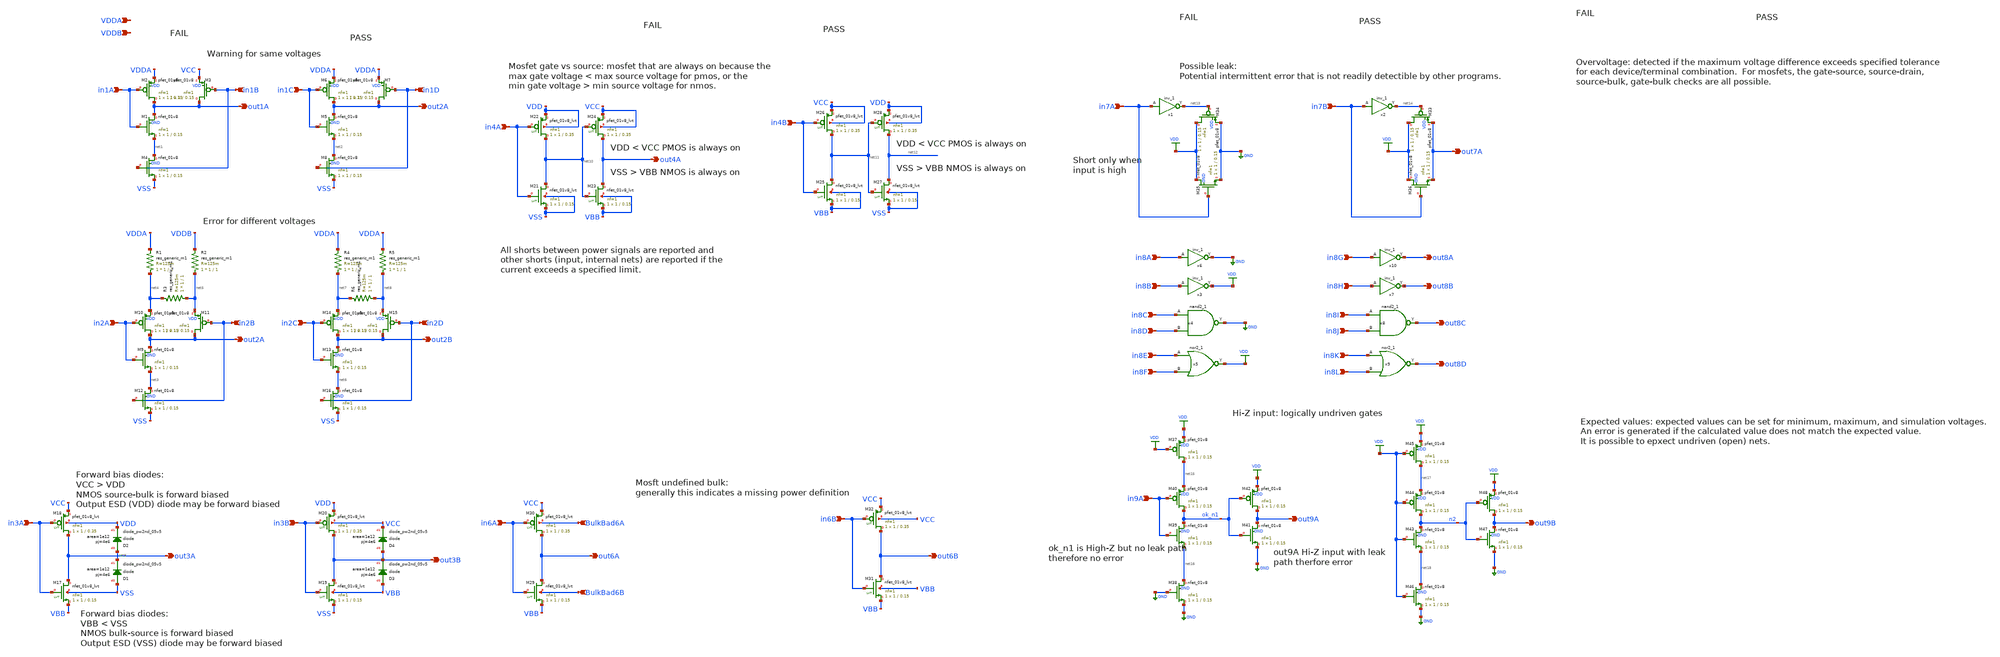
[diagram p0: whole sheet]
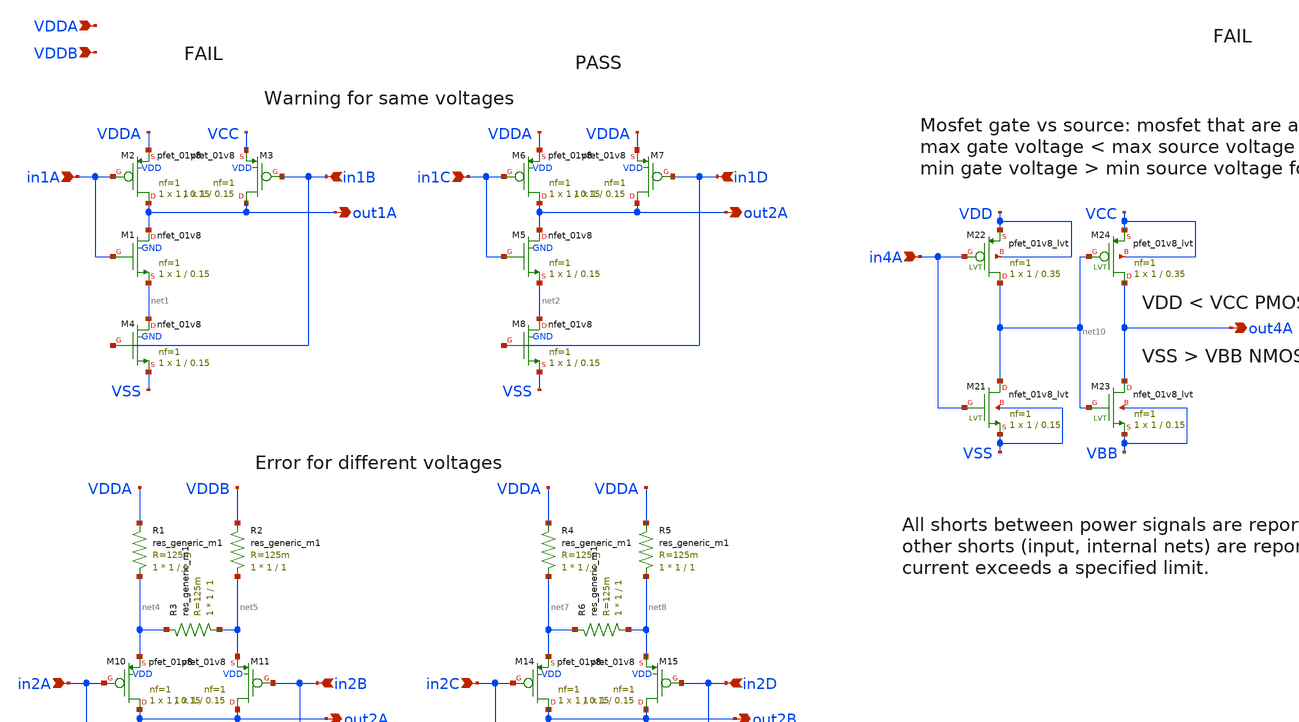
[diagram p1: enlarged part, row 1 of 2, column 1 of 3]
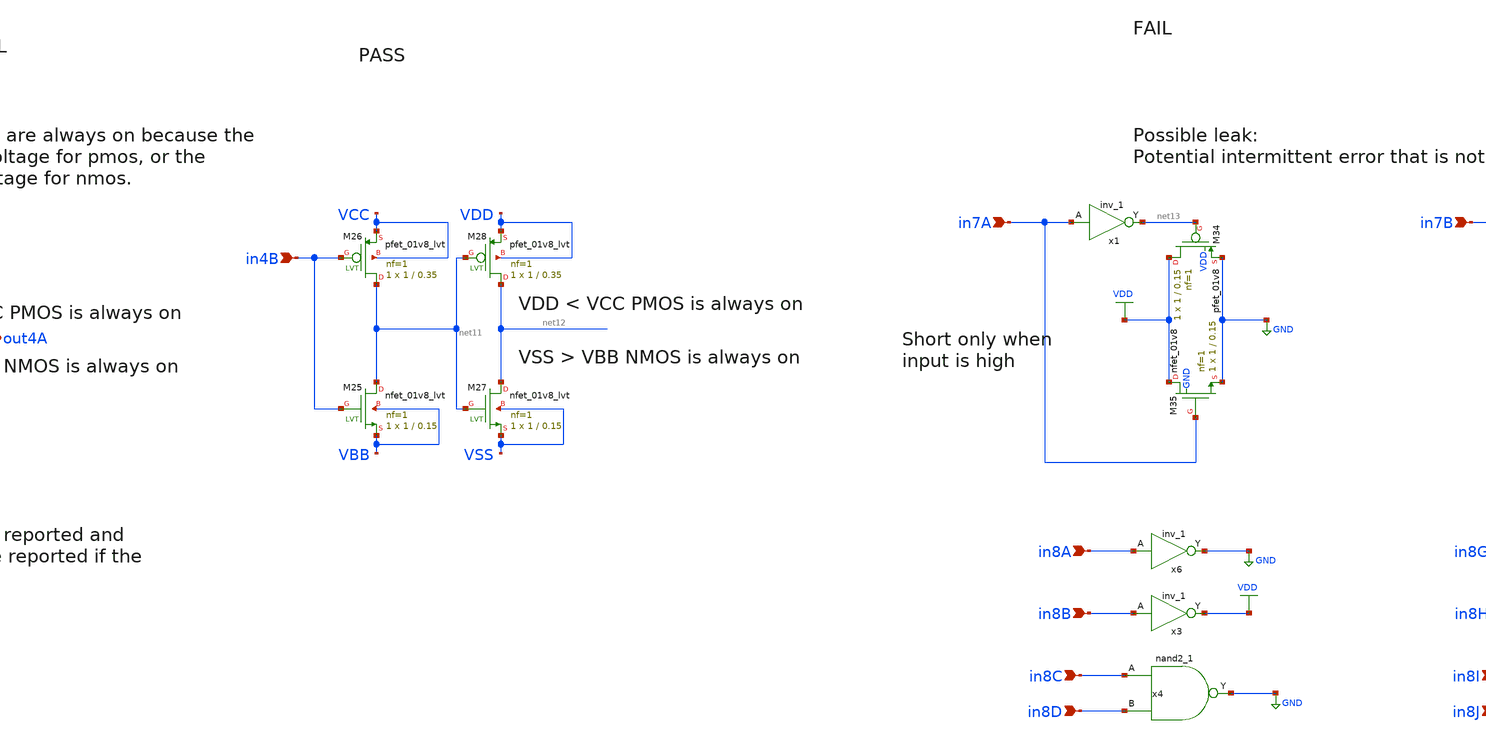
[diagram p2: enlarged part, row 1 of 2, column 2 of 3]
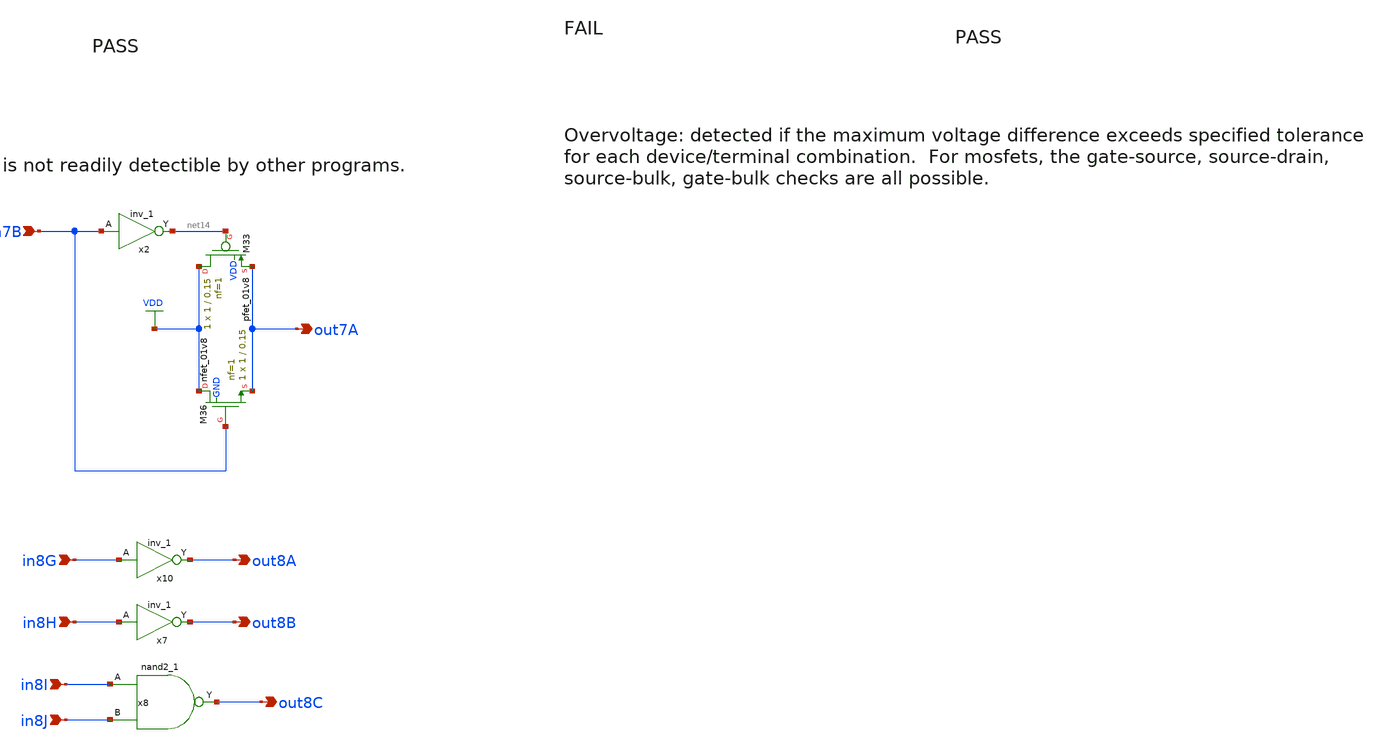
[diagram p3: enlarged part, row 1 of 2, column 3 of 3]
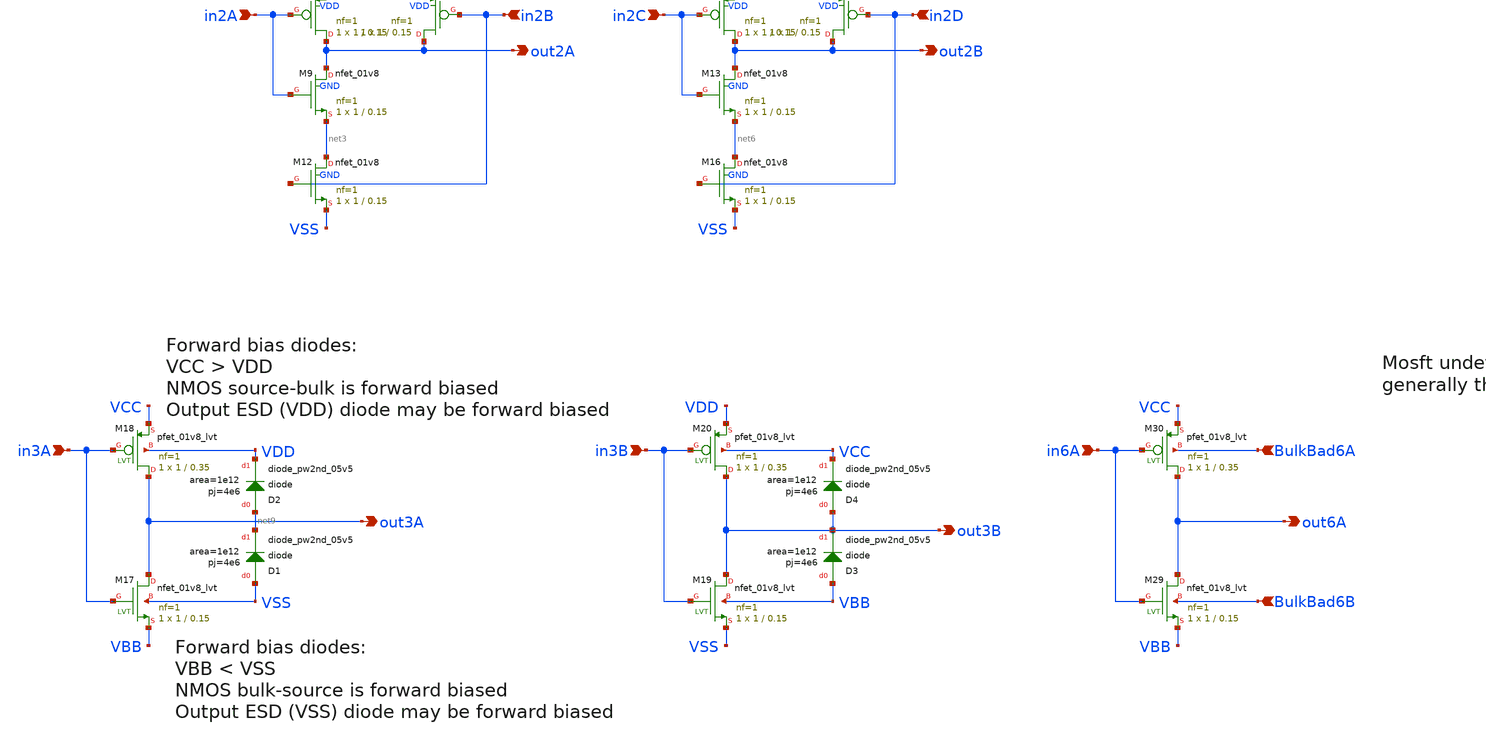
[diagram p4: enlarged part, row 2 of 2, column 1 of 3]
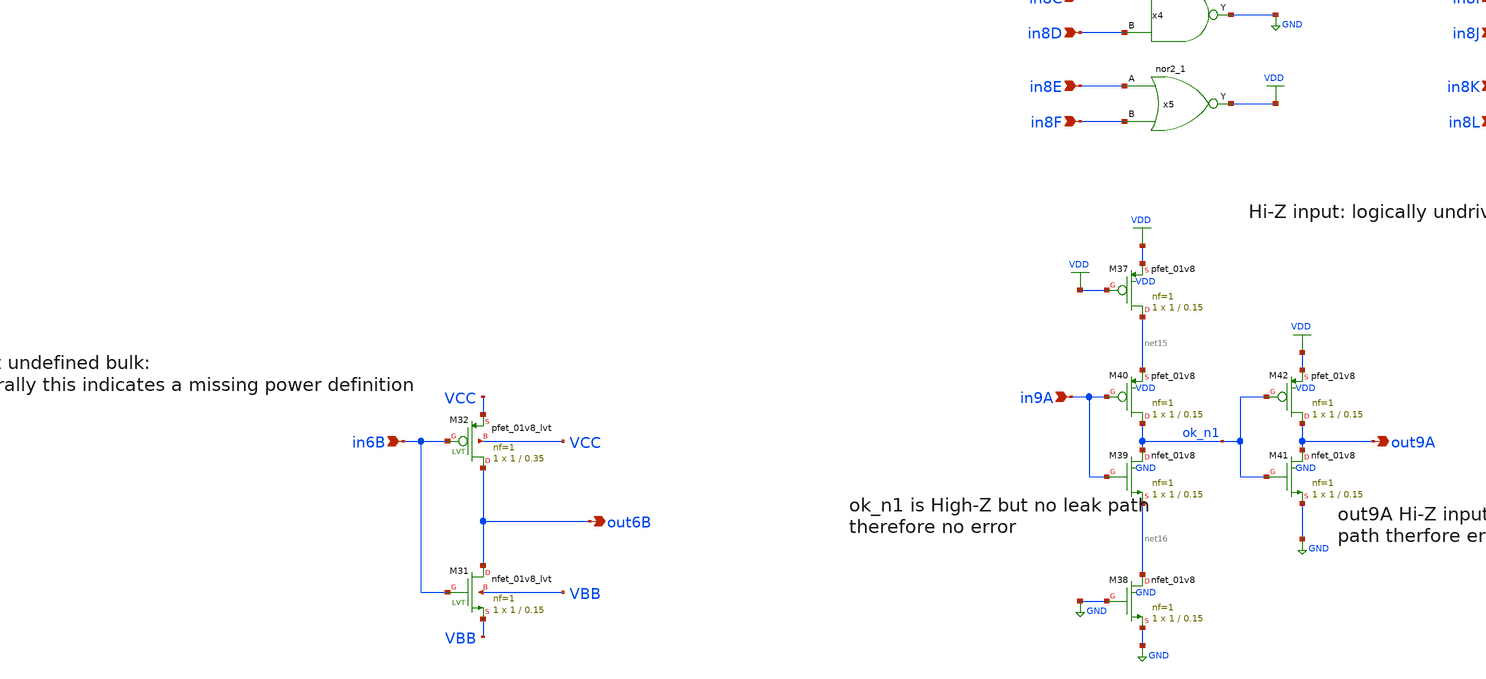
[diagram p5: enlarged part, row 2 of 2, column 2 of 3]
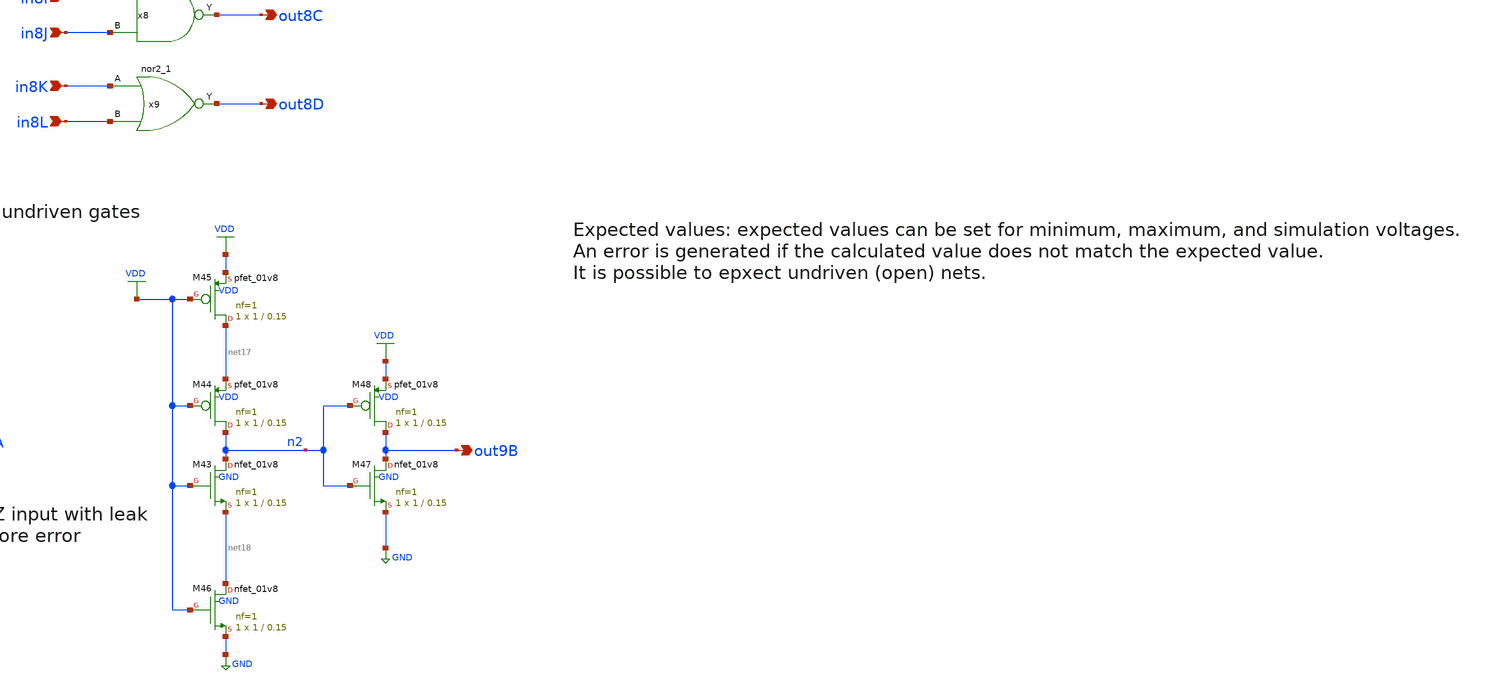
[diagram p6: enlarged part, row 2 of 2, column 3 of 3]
** sch_path: src/xe/test_cases/cvc_errors.sch
**.subckt cvc_errors in1A in1B in1C in1D in2A in2B in2C in2D out1A out2A out3A out2B in3A in3B out2A
*+ out3B in4A out4A in4B out7A in6A in6B out6A out6B in7A in7B in8A in8B in8C in8D in8E in8F in8G in8H in8I
*+ in8J in8K in8L out8A out8B out8C out8D in9A out9A out9B BulkBad6A BulkBad6B VDDB VDDA
*.ipin in1A
*.ipin in1B
*.ipin in1C
*.ipin in1D
*.ipin in2A
*.ipin in2B
*.ipin in2C
*.ipin in2D
*.opin out1A
*.opin out2A
*.opin out3A
*.opin out2B
*.ipin in3A
*.ipin in3B
*.opin out2A
*.opin out3B
*.ipin in4A
*.opin out4A
*.ipin in4B
*.opin out7A
*.ipin in6A
*.ipin in6B
*.opin out6A
*.opin out6B
*.ipin in7A
*.ipin in7B
*.ipin in8A
*.ipin in8B
*.ipin in8C
*.ipin in8D
*.ipin in8E
*.ipin in8F
*.ipin in8G
*.ipin in8H
*.ipin in8I
*.ipin in8J
*.ipin in8K
*.ipin in8L
*.opin out8A
*.opin out8B
*.opin out8C
*.opin out8D
*.ipin in9A
*.opin out9A
*.opin out9B
*.ipin BulkBad6A
*.ipin BulkBad6B
*.ipin VDDB
*.ipin VDDA
XM1 out1A in1A net1 GND sky130_fd_pr__nfet_01v8 L=0.15 W=1 nf=1 ad='int((nf+1)/2) * W/nf * 0.29' as='int((nf+2)/2) * W/nf * 0.29'
+ pd='2*int((nf+1)/2) * (W/nf + 0.29)' ps='2*int((nf+2)/2) * (W/nf + 0.29)' nrd='0.29 / W' nrs='0.29 / W'
+ sa=0 sb=0 sd=0 mult=1 m=1
XM2 out1A in1A VDDA VDD sky130_fd_pr__pfet_01v8 L=0.15 W=1 nf=1 ad='int((nf+1)/2) * W/nf * 0.29' as='int((nf+2)/2) * W/nf * 0.29'
+ pd='2*int((nf+1)/2) * (W/nf + 0.29)' ps='2*int((nf+2)/2) * (W/nf + 0.29)' nrd='0.29 / W' nrs='0.29 / W'
+ sa=0 sb=0 sd=0 mult=1 m=1
XM3 out1A in1B VCC VDD sky130_fd_pr__pfet_01v8 L=0.15 W=1 nf=1 ad='int((nf+1)/2) * W/nf * 0.29' as='int((nf+2)/2) * W/nf * 0.29'
+ pd='2*int((nf+1)/2) * (W/nf + 0.29)' ps='2*int((nf+2)/2) * (W/nf + 0.29)' nrd='0.29 / W' nrs='0.29 / W'
+ sa=0 sb=0 sd=0 mult=1 m=1
XM4 net1 in1B VSS GND sky130_fd_pr__nfet_01v8 L=0.15 W=1 nf=1 ad='int((nf+1)/2) * W/nf * 0.29' as='int((nf+2)/2) * W/nf * 0.29'
+ pd='2*int((nf+1)/2) * (W/nf + 0.29)' ps='2*int((nf+2)/2) * (W/nf + 0.29)' nrd='0.29 / W' nrs='0.29 / W'
+ sa=0 sb=0 sd=0 mult=1 m=1
XM5 out2A in1C net2 GND sky130_fd_pr__nfet_01v8 L=0.15 W=1 nf=1 ad='int((nf+1)/2) * W/nf * 0.29' as='int((nf+2)/2) * W/nf * 0.29'
+ pd='2*int((nf+1)/2) * (W/nf + 0.29)' ps='2*int((nf+2)/2) * (W/nf + 0.29)' nrd='0.29 / W' nrs='0.29 / W'
+ sa=0 sb=0 sd=0 mult=1 m=1
XM6 out2A in1C VDDA VDD sky130_fd_pr__pfet_01v8 L=0.15 W=1 nf=1 ad='int((nf+1)/2) * W/nf * 0.29' as='int((nf+2)/2) * W/nf * 0.29'
+ pd='2*int((nf+1)/2) * (W/nf + 0.29)' ps='2*int((nf+2)/2) * (W/nf + 0.29)' nrd='0.29 / W' nrs='0.29 / W'
+ sa=0 sb=0 sd=0 mult=1 m=1
XM7 out2A in1D VDDA VDD sky130_fd_pr__pfet_01v8 L=0.15 W=1 nf=1 ad='int((nf+1)/2) * W/nf * 0.29' as='int((nf+2)/2) * W/nf * 0.29'
+ pd='2*int((nf+1)/2) * (W/nf + 0.29)' ps='2*int((nf+2)/2) * (W/nf + 0.29)' nrd='0.29 / W' nrs='0.29 / W'
+ sa=0 sb=0 sd=0 mult=1 m=1
XM8 net2 in1D VSS GND sky130_fd_pr__nfet_01v8 L=0.15 W=1 nf=1 ad='int((nf+1)/2) * W/nf * 0.29' as='int((nf+2)/2) * W/nf * 0.29'
+ pd='2*int((nf+1)/2) * (W/nf + 0.29)' ps='2*int((nf+2)/2) * (W/nf + 0.29)' nrd='0.29 / W' nrs='0.29 / W'
+ sa=0 sb=0 sd=0 mult=1 m=1
R1 net4 VDDA sky130_fd_pr__res_generic_m1 W=1 L=1 m=1
XM9 out2A in2A net3 GND sky130_fd_pr__nfet_01v8 L=0.15 W=1 nf=1 ad='int((nf+1)/2) * W/nf * 0.29' as='int((nf+2)/2) * W/nf * 0.29'
+ pd='2*int((nf+1)/2) * (W/nf + 0.29)' ps='2*int((nf+2)/2) * (W/nf + 0.29)' nrd='0.29 / W' nrs='0.29 / W'
+ sa=0 sb=0 sd=0 mult=1 m=1
XM10 out2A in2A net4 VDD sky130_fd_pr__pfet_01v8 L=0.15 W=1 nf=1 ad='int((nf+1)/2) * W/nf * 0.29' as='int((nf+2)/2) * W/nf * 0.29'
+ pd='2*int((nf+1)/2) * (W/nf + 0.29)' ps='2*int((nf+2)/2) * (W/nf + 0.29)' nrd='0.29 / W' nrs='0.29 / W'
+ sa=0 sb=0 sd=0 mult=1 m=1
XM11 out2A in2B net5 VDD sky130_fd_pr__pfet_01v8 L=0.15 W=1 nf=1 ad='int((nf+1)/2) * W/nf * 0.29' as='int((nf+2)/2) * W/nf * 0.29'
+ pd='2*int((nf+1)/2) * (W/nf + 0.29)' ps='2*int((nf+2)/2) * (W/nf + 0.29)' nrd='0.29 / W' nrs='0.29 / W'
+ sa=0 sb=0 sd=0 mult=1 m=1
XM12 net3 in2B VSS GND sky130_fd_pr__nfet_01v8 L=0.15 W=1 nf=1 ad='int((nf+1)/2) * W/nf * 0.29' as='int((nf+2)/2) * W/nf * 0.29'
+ pd='2*int((nf+1)/2) * (W/nf + 0.29)' ps='2*int((nf+2)/2) * (W/nf + 0.29)' nrd='0.29 / W' nrs='0.29 / W'
+ sa=0 sb=0 sd=0 mult=1 m=1
R2 net5 VDDB sky130_fd_pr__res_generic_m1 W=1 L=1 m=1
R3 net5 net4 sky130_fd_pr__res_generic_m1 W=1 L=1 m=1
R4 net7 VDDA sky130_fd_pr__res_generic_m1 W=1 L=1 m=1
XM13 out2B in2C net6 GND sky130_fd_pr__nfet_01v8 L=0.15 W=1 nf=1 ad='int((nf+1)/2) * W/nf * 0.29' as='int((nf+2)/2) * W/nf * 0.29'
+ pd='2*int((nf+1)/2) * (W/nf + 0.29)' ps='2*int((nf+2)/2) * (W/nf + 0.29)' nrd='0.29 / W' nrs='0.29 / W'
+ sa=0 sb=0 sd=0 mult=1 m=1
XM14 out2B in2C net7 VDD sky130_fd_pr__pfet_01v8 L=0.15 W=1 nf=1 ad='int((nf+1)/2) * W/nf * 0.29' as='int((nf+2)/2) * W/nf * 0.29'
+ pd='2*int((nf+1)/2) * (W/nf + 0.29)' ps='2*int((nf+2)/2) * (W/nf + 0.29)' nrd='0.29 / W' nrs='0.29 / W'
+ sa=0 sb=0 sd=0 mult=1 m=1
XM15 out2B in2D net8 VDD sky130_fd_pr__pfet_01v8 L=0.15 W=1 nf=1 ad='int((nf+1)/2) * W/nf * 0.29' as='int((nf+2)/2) * W/nf * 0.29'
+ pd='2*int((nf+1)/2) * (W/nf + 0.29)' ps='2*int((nf+2)/2) * (W/nf + 0.29)' nrd='0.29 / W' nrs='0.29 / W'
+ sa=0 sb=0 sd=0 mult=1 m=1
XM16 net6 in2D VSS GND sky130_fd_pr__nfet_01v8 L=0.15 W=1 nf=1 ad='int((nf+1)/2) * W/nf * 0.29' as='int((nf+2)/2) * W/nf * 0.29'
+ pd='2*int((nf+1)/2) * (W/nf + 0.29)' ps='2*int((nf+2)/2) * (W/nf + 0.29)' nrd='0.29 / W' nrs='0.29 / W'
+ sa=0 sb=0 sd=0 mult=1 m=1
R5 net8 VDDA sky130_fd_pr__res_generic_m1 W=1 L=1 m=1
R6 net8 net7 sky130_fd_pr__res_generic_m1 W=1 L=1 m=1
XM17 out3A in3A VBB VSS sky130_fd_pr__nfet_01v8_lvt L=0.15 W=1 nf=1 ad='int((nf+1)/2) * W/nf * 0.29'
+ as='int((nf+2)/2) * W/nf * 0.29' pd='2*int((nf+1)/2) * (W/nf + 0.29)' ps='2*int((nf+2)/2) * (W/nf + 0.29)'
+ nrd='0.29 / W' nrs='0.29 / W' sa=0 sb=0 sd=0 mult=1 m=1
XM18 out3A in3A VCC VDD sky130_fd_pr__pfet_01v8_lvt L=0.35 W=1 nf=1 ad='int((nf+1)/2) * W/nf * 0.29'
+ as='int((nf+2)/2) * W/nf * 0.29' pd='2*int((nf+1)/2) * (W/nf + 0.29)' ps='2*int((nf+2)/2) * (W/nf + 0.29)'
+ nrd='0.29 / W' nrs='0.29 / W' sa=0 sb=0 sd=0 mult=1 m=1
XD1 VSS net9 sky130_fd_pr__diode_pw2nd_05v5 area=1e12 pj=4e6
XD2 net9 VDD sky130_fd_pr__diode_pw2nd_05v5 area=1e12 pj=4e6
XM19 out3B in3B VSS VBB sky130_fd_pr__nfet_01v8_lvt L=0.15 W=1 nf=1 ad='int((nf+1)/2) * W/nf * 0.29'
+ as='int((nf+2)/2) * W/nf * 0.29' pd='2*int((nf+1)/2) * (W/nf + 0.29)' ps='2*int((nf+2)/2) * (W/nf + 0.29)'
+ nrd='0.29 / W' nrs='0.29 / W' sa=0 sb=0 sd=0 mult=1 m=1
XM20 out3B in3B VDD VCC sky130_fd_pr__pfet_01v8_lvt L=0.35 W=1 nf=1 ad='int((nf+1)/2) * W/nf * 0.29'
+ as='int((nf+2)/2) * W/nf * 0.29' pd='2*int((nf+1)/2) * (W/nf + 0.29)' ps='2*int((nf+2)/2) * (W/nf + 0.29)'
+ nrd='0.29 / W' nrs='0.29 / W' sa=0 sb=0 sd=0 mult=1 m=1
XD3 VBB out3B sky130_fd_pr__diode_pw2nd_05v5 area=1e12 pj=4e6
XD4 out3B VCC sky130_fd_pr__diode_pw2nd_05v5 area=1e12 pj=4e6
XM21 net10 in4A VSS VSS sky130_fd_pr__nfet_01v8_lvt L=0.15 W=1 nf=1 ad='int((nf+1)/2) * W/nf * 0.29'
+ as='int((nf+2)/2) * W/nf * 0.29' pd='2*int((nf+1)/2) * (W/nf + 0.29)' ps='2*int((nf+2)/2) * (W/nf + 0.29)'
+ nrd='0.29 / W' nrs='0.29 / W' sa=0 sb=0 sd=0 mult=1 m=1
XM22 net10 in4A VDD VDD sky130_fd_pr__pfet_01v8_lvt L=0.35 W=1 nf=1 ad='int((nf+1)/2) * W/nf * 0.29'
+ as='int((nf+2)/2) * W/nf * 0.29' pd='2*int((nf+1)/2) * (W/nf + 0.29)' ps='2*int((nf+2)/2) * (W/nf + 0.29)'
+ nrd='0.29 / W' nrs='0.29 / W' sa=0 sb=0 sd=0 mult=1 m=1
XM23 out4A net10 VBB VBB sky130_fd_pr__nfet_01v8_lvt L=0.15 W=1 nf=1 ad='int((nf+1)/2) * W/nf * 0.29'
+ as='int((nf+2)/2) * W/nf * 0.29' pd='2*int((nf+1)/2) * (W/nf + 0.29)' ps='2*int((nf+2)/2) * (W/nf + 0.29)'
+ nrd='0.29 / W' nrs='0.29 / W' sa=0 sb=0 sd=0 mult=1 m=1
XM24 out4A net10 VCC VCC sky130_fd_pr__pfet_01v8_lvt L=0.35 W=1 nf=1 ad='int((nf+1)/2) * W/nf * 0.29'
+ as='int((nf+2)/2) * W/nf * 0.29' pd='2*int((nf+1)/2) * (W/nf + 0.29)' ps='2*int((nf+2)/2) * (W/nf + 0.29)'
+ nrd='0.29 / W' nrs='0.29 / W' sa=0 sb=0 sd=0 mult=1 m=1
XM25 net11 in4B VBB VBB sky130_fd_pr__nfet_01v8_lvt L=0.15 W=1 nf=1 ad='int((nf+1)/2) * W/nf * 0.29'
+ as='int((nf+2)/2) * W/nf * 0.29' pd='2*int((nf+1)/2) * (W/nf + 0.29)' ps='2*int((nf+2)/2) * (W/nf + 0.29)'
+ nrd='0.29 / W' nrs='0.29 / W' sa=0 sb=0 sd=0 mult=1 m=1
XM26 net11 in4B VCC VCC sky130_fd_pr__pfet_01v8_lvt L=0.35 W=1 nf=1 ad='int((nf+1)/2) * W/nf * 0.29'
+ as='int((nf+2)/2) * W/nf * 0.29' pd='2*int((nf+1)/2) * (W/nf + 0.29)' ps='2*int((nf+2)/2) * (W/nf + 0.29)'
+ nrd='0.29 / W' nrs='0.29 / W' sa=0 sb=0 sd=0 mult=1 m=1
XM27 net12 net11 VSS VSS sky130_fd_pr__nfet_01v8_lvt L=0.15 W=1 nf=1 ad='int((nf+1)/2) * W/nf * 0.29'
+ as='int((nf+2)/2) * W/nf * 0.29' pd='2*int((nf+1)/2) * (W/nf + 0.29)' ps='2*int((nf+2)/2) * (W/nf + 0.29)'
+ nrd='0.29 / W' nrs='0.29 / W' sa=0 sb=0 sd=0 mult=1 m=1
XM28 net12 net11 VDD VDD sky130_fd_pr__pfet_01v8_lvt L=0.35 W=1 nf=1 ad='int((nf+1)/2) * W/nf * 0.29'
+ as='int((nf+2)/2) * W/nf * 0.29' pd='2*int((nf+1)/2) * (W/nf + 0.29)' ps='2*int((nf+2)/2) * (W/nf + 0.29)'
+ nrd='0.29 / W' nrs='0.29 / W' sa=0 sb=0 sd=0 mult=1 m=1
XM29 out6A in6A VBB BulkBad6B sky130_fd_pr__nfet_01v8_lvt L=0.15 W=1 nf=1 ad='int((nf+1)/2) * W/nf * 0.29'
+ as='int((nf+2)/2) * W/nf * 0.29' pd='2*int((nf+1)/2) * (W/nf + 0.29)' ps='2*int((nf+2)/2) * (W/nf + 0.29)'
+ nrd='0.29 / W' nrs='0.29 / W' sa=0 sb=0 sd=0 mult=1 m=1
XM30 out6A in6A VCC BulkBad6A sky130_fd_pr__pfet_01v8_lvt L=0.35 W=1 nf=1 ad='int((nf+1)/2) * W/nf * 0.29'
+ as='int((nf+2)/2) * W/nf * 0.29' pd='2*int((nf+1)/2) * (W/nf + 0.29)' ps='2*int((nf+2)/2) * (W/nf + 0.29)'
+ nrd='0.29 / W' nrs='0.29 / W' sa=0 sb=0 sd=0 mult=1 m=1
XM31 out6B in6B VBB VBB sky130_fd_pr__nfet_01v8_lvt L=0.15 W=1 nf=1 ad='int((nf+1)/2) * W/nf * 0.29'
+ as='int((nf+2)/2) * W/nf * 0.29' pd='2*int((nf+1)/2) * (W/nf + 0.29)' ps='2*int((nf+2)/2) * (W/nf + 0.29)'
+ nrd='0.29 / W' nrs='0.29 / W' sa=0 sb=0 sd=0 mult=1 m=1
XM32 out6B in6B VCC VCC sky130_fd_pr__pfet_01v8_lvt L=0.35 W=1 nf=1 ad='int((nf+1)/2) * W/nf * 0.29'
+ as='int((nf+2)/2) * W/nf * 0.29' pd='2*int((nf+1)/2) * (W/nf + 0.29)' ps='2*int((nf+2)/2) * (W/nf + 0.29)'
+ nrd='0.29 / W' nrs='0.29 / W' sa=0 sb=0 sd=0 mult=1 m=1
XM34 VDD net13 GND VDD sky130_fd_pr__pfet_01v8 L=0.15 W=1 nf=1 ad='int((nf+1)/2) * W/nf * 0.29' as='int((nf+2)/2) * W/nf * 0.29'
+ pd='2*int((nf+1)/2) * (W/nf + 0.29)' ps='2*int((nf+2)/2) * (W/nf + 0.29)' nrd='0.29 / W' nrs='0.29 / W'
+ sa=0 sb=0 sd=0 mult=1 m=1
XM35 VDD in7A GND GND sky130_fd_pr__nfet_01v8 L=0.15 W=1 nf=1 ad='int((nf+1)/2) * W/nf * 0.29' as='int((nf+2)/2) * W/nf * 0.29'
+ pd='2*int((nf+1)/2) * (W/nf + 0.29)' ps='2*int((nf+2)/2) * (W/nf + 0.29)' nrd='0.29 / W' nrs='0.29 / W'
+ sa=0 sb=0 sd=0 mult=1 m=1
x1 in7A VGND VNB VPB VPWR net13 sky130_fd_sc_hd__inv_1
XM33 VDD net14 out7A VDD sky130_fd_pr__pfet_01v8 L=0.15 W=1 nf=1 ad='int((nf+1)/2) * W/nf * 0.29' as='int((nf+2)/2) * W/nf * 0.29'
+ pd='2*int((nf+1)/2) * (W/nf + 0.29)' ps='2*int((nf+2)/2) * (W/nf + 0.29)' nrd='0.29 / W' nrs='0.29 / W'
+ sa=0 sb=0 sd=0 mult=1 m=1
XM36 VDD in7B out7A GND sky130_fd_pr__nfet_01v8 L=0.15 W=1 nf=1 ad='int((nf+1)/2) * W/nf * 0.29' as='int((nf+2)/2) * W/nf * 0.29'
+ pd='2*int((nf+1)/2) * (W/nf + 0.29)' ps='2*int((nf+2)/2) * (W/nf + 0.29)' nrd='0.29 / W' nrs='0.29 / W'
+ sa=0 sb=0 sd=0 mult=1 m=1
x2 in7B VGND VNB VPB VPWR net14 sky130_fd_sc_hd__inv_1
x3 in8B VGND VNB VPB VPWR VDD sky130_fd_sc_hd__inv_1
x4 in8C in8D VGND VNB VPB VPWR GND sky130_fd_sc_hd__nand2_1
x5 in8E in8F VGND VNB VPB VPWR VDD sky130_fd_sc_hd__nor2_1
x6 in8A VGND VNB VPB VPWR GND sky130_fd_sc_hd__inv_1
x7 in8H VGND VNB VPB VPWR out8B sky130_fd_sc_hd__inv_1
x8 in8I in8J VGND VNB VPB VPWR out8C sky130_fd_sc_hd__nand2_1
x9 in8K in8L VGND VNB VPB VPWR out8D sky130_fd_sc_hd__nor2_1
x10 in8G VGND VNB VPB VPWR out8A sky130_fd_sc_hd__inv_1
XM39 ok_n1 in9A net16 GND sky130_fd_pr__nfet_01v8 L=0.15 W=1 nf=1 ad='int((nf+1)/2) * W/nf * 0.29' as='int((nf+2)/2) * W/nf * 0.29'
+ pd='2*int((nf+1)/2) * (W/nf + 0.29)' ps='2*int((nf+2)/2) * (W/nf + 0.29)' nrd='0.29 / W' nrs='0.29 / W'
+ sa=0 sb=0 sd=0 mult=1 m=1
XM40 ok_n1 in9A net15 VDD sky130_fd_pr__pfet_01v8 L=0.15 W=1 nf=1 ad='int((nf+1)/2) * W/nf * 0.29' as='int((nf+2)/2) * W/nf * 0.29'
+ pd='2*int((nf+1)/2) * (W/nf + 0.29)' ps='2*int((nf+2)/2) * (W/nf + 0.29)' nrd='0.29 / W' nrs='0.29 / W'
+ sa=0 sb=0 sd=0 mult=1 m=1
XM37 net15 VDD VDD VDD sky130_fd_pr__pfet_01v8 L=0.15 W=1 nf=1 ad='int((nf+1)/2) * W/nf * 0.29' as='int((nf+2)/2) * W/nf * 0.29'
+ pd='2*int((nf+1)/2) * (W/nf + 0.29)' ps='2*int((nf+2)/2) * (W/nf + 0.29)' nrd='0.29 / W' nrs='0.29 / W'
+ sa=0 sb=0 sd=0 mult=1 m=1
XM38 net16 GND GND GND sky130_fd_pr__nfet_01v8 L=0.15 W=1 nf=1 ad='int((nf+1)/2) * W/nf * 0.29' as='int((nf+2)/2) * W/nf * 0.29'
+ pd='2*int((nf+1)/2) * (W/nf + 0.29)' ps='2*int((nf+2)/2) * (W/nf + 0.29)' nrd='0.29 / W' nrs='0.29 / W'
+ sa=0 sb=0 sd=0 mult=1 m=1
XM41 out9A ok_n1 GND GND sky130_fd_pr__nfet_01v8 L=0.15 W=1 nf=1 ad='int((nf+1)/2) * W/nf * 0.29' as='int((nf+2)/2) * W/nf * 0.29'
+ pd='2*int((nf+1)/2) * (W/nf + 0.29)' ps='2*int((nf+2)/2) * (W/nf + 0.29)' nrd='0.29 / W' nrs='0.29 / W'
+ sa=0 sb=0 sd=0 mult=1 m=1
XM42 out9A ok_n1 VDD VDD sky130_fd_pr__pfet_01v8 L=0.15 W=1 nf=1 ad='int((nf+1)/2) * W/nf * 0.29' as='int((nf+2)/2) * W/nf * 0.29'
+ pd='2*int((nf+1)/2) * (W/nf + 0.29)' ps='2*int((nf+2)/2) * (W/nf + 0.29)' nrd='0.29 / W' nrs='0.29 / W'
+ sa=0 sb=0 sd=0 mult=1 m=1
XM43 n2 VDD net18 GND sky130_fd_pr__nfet_01v8 L=0.15 W=1 nf=1 ad='int((nf+1)/2) * W/nf * 0.29' as='int((nf+2)/2) * W/nf * 0.29'
+ pd='2*int((nf+1)/2) * (W/nf + 0.29)' ps='2*int((nf+2)/2) * (W/nf + 0.29)' nrd='0.29 / W' nrs='0.29 / W'
+ sa=0 sb=0 sd=0 mult=1 m=1
XM44 n2 VDD net17 VDD sky130_fd_pr__pfet_01v8 L=0.15 W=1 nf=1 ad='int((nf+1)/2) * W/nf * 0.29' as='int((nf+2)/2) * W/nf * 0.29'
+ pd='2*int((nf+1)/2) * (W/nf + 0.29)' ps='2*int((nf+2)/2) * (W/nf + 0.29)' nrd='0.29 / W' nrs='0.29 / W'
+ sa=0 sb=0 sd=0 mult=1 m=1
XM45 net17 VDD VDD VDD sky130_fd_pr__pfet_01v8 L=0.15 W=1 nf=1 ad='int((nf+1)/2) * W/nf * 0.29' as='int((nf+2)/2) * W/nf * 0.29'
+ pd='2*int((nf+1)/2) * (W/nf + 0.29)' ps='2*int((nf+2)/2) * (W/nf + 0.29)' nrd='0.29 / W' nrs='0.29 / W'
+ sa=0 sb=0 sd=0 mult=1 m=1
XM46 net18 VDD GND GND sky130_fd_pr__nfet_01v8 L=0.15 W=1 nf=1 ad='int((nf+1)/2) * W/nf * 0.29' as='int((nf+2)/2) * W/nf * 0.29'
+ pd='2*int((nf+1)/2) * (W/nf + 0.29)' ps='2*int((nf+2)/2) * (W/nf + 0.29)' nrd='0.29 / W' nrs='0.29 / W'
+ sa=0 sb=0 sd=0 mult=1 m=1
XM47 out9B n2 GND GND sky130_fd_pr__nfet_01v8 L=0.15 W=1 nf=1 ad='int((nf+1)/2) * W/nf * 0.29' as='int((nf+2)/2) * W/nf * 0.29'
+ pd='2*int((nf+1)/2) * (W/nf + 0.29)' ps='2*int((nf+2)/2) * (W/nf + 0.29)' nrd='0.29 / W' nrs='0.29 / W'
+ sa=0 sb=0 sd=0 mult=1 m=1
XM48 out9B n2 VDD VDD sky130_fd_pr__pfet_01v8 L=0.15 W=1 nf=1 ad='int((nf+1)/2) * W/nf * 0.29' as='int((nf+2)/2) * W/nf * 0.29'
+ pd='2*int((nf+1)/2) * (W/nf + 0.29)' ps='2*int((nf+2)/2) * (W/nf + 0.29)' nrd='0.29 / W' nrs='0.29 / W'
+ sa=0 sb=0 sd=0 mult=1 m=1
**** begin user architecture code


.SUBCKT sky130_fd_sc_hd__inv_1 A VGND VNB VPB VPWR Y
*.PININFO A:I VGND:I VNB:I VPB:I VPWR:I Y:O
MMIN1 Y A VGND VNB nfet_01v8 m=1 w=0.65 l=0.15 mult=1 sa=0.265  sb=0.265 sd=0.28 topography=normal
+ area=0.063 perim=1.14
MMIP1 Y A VPWR VPB pfet_01v8_hvt m=1 w=1.0 l=0.15 mult=1 sa=0.265  sb=0.265 sd=0.28
+ topography=normal area=0.063 perim=1.14
.ENDS sky130_fd_sc_hd__inv_1

.SUBCKT sky130_fd_sc_hd__nand2_1 A B VGND VNB VPB VPWR Y
*.PININFO A:I B:I VGND:I VNB:I VPB:I VPWR:I Y:O
MMP0 Y A VPWR VPB pfet_01v8_hvt m=1 w=1.0 l=0.15 mult=1 sa=0.265  sb=0.265 sd=0.28 topography=normal
+ area=0.063 perim=1.14
MMP1 Y B VPWR VPB pfet_01v8_hvt m=1 w=1.0 l=0.15 mult=1 sa=0.265  sb=0.265 sd=0.28 topography=normal
+ area=0.063 perim=1.14
MMN0 Y A sndA VNB nfet_01v8 m=1 w=0.65 l=0.15 mult=1 sa=0.265 sb=0.265  sd=0.28 topography=normal
+ area=0.063 perim=1.14
MMN1 sndA B VGND VNB nfet_01v8 m=1 w=0.65 l=0.15 mult=1 sa=0.265  sb=0.265 sd=0.28 topography=normal
+ area=0.063 perim=1.14
.ENDS sky130_fd_sc_hd__nand2_1

.SUBCKT sky130_fd_sc_hd__nor2_1 A B VGND VNB VPB VPWR Y
*.PININFO A:I B:I VGND:I VNB:I VPB:I VPWR:I Y:O
MMP0 VPWR A sndPA VPB pfet_01v8_hvt m=1 w=1.0 l=0.15 mult=1 sa=0.265  sb=0.265 sd=0.28
+ topography=normal area=0.063 perim=1.14
MMP1 sndPA B Y VPB pfet_01v8_hvt m=1 w=1.0 l=0.15 mult=1 sa=0.265  sb=0.265 sd=0.28
+ topography=normal area=0.063 perim=1.14
MMN0 Y A VGND VNB nfet_01v8 m=1 w=0.65 l=0.15 mult=1 sa=0.265 sb=0.265  sd=0.28 topography=normal
+ area=0.063 perim=1.14
MMN1 Y B VGND VNB nfet_01v8 m=1 w=0.65 l=0.15 mult=1 sa=0.265 sb=0.265  sd=0.28 topography=normal
+ area=0.063 perim=1.14
.ENDS sky130_fd_sc_hd__nor2_1


**** end user architecture code
**.ends
.GLOBAL GND
.GLOBAL VDD
.end
